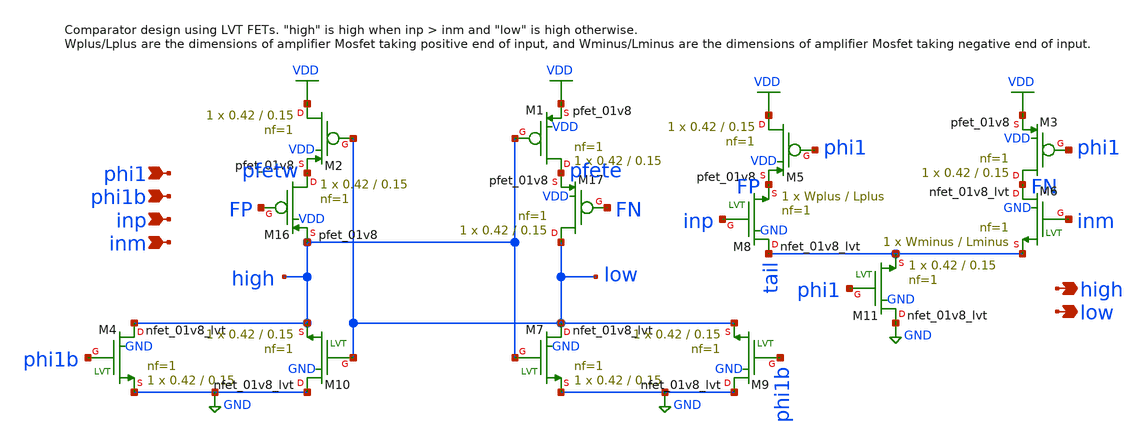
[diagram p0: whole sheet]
** sch_path: xschem/tryandtest/comparator_single_tail.sch
**.subckt comparator_single_tail phi1 high phi1b inp inm low
*.ipin phi1
*.opin high
*.ipin phi1b
*.ipin inp
*.ipin inm
*.opin low
XM1 pfete high VDD VDD sky130_fd_pr__pfet_01v8 L=0.15 W=0.42 nf=1 ad='int((nf+1)/2) * W/nf * 0.29' as='int((nf+2)/2) * W/nf * 0.29'
+ pd='2*int((nf+1)/2) * (W/nf + 0.29)' ps='2*int((nf+2)/2) * (W/nf + 0.29)' nrd='0.29 / W' nrs='0.29 / W'
+ sa=0 sb=0 sd=0 mult=1 m=1
XM2 VDD low pfetw VDD sky130_fd_pr__pfet_01v8 L=0.15 W=0.42 nf=1 ad='int((nf+1)/2) * W/nf * 0.29' as='int((nf+2)/2) * W/nf * 0.29'
+ pd='2*int((nf+1)/2) * (W/nf + 0.29)' ps='2*int((nf+2)/2) * (W/nf + 0.29)' nrd='0.29 / W' nrs='0.29 / W'
+ sa=0 sb=0 sd=0 mult=1 m=1
XM16 pfetw FP high VDD sky130_fd_pr__pfet_01v8 L=0.15 W=0.42 nf=1 ad='int((nf+1)/2) * W/nf * 0.29' as='int((nf+2)/2) * W/nf * 0.29'
+ pd='2*int((nf+1)/2) * (W/nf + 0.29)' ps='2*int((nf+2)/2) * (W/nf + 0.29)' nrd='0.29 / W' nrs='0.29 / W'
+ sa=0 sb=0 sd=0 mult=1 m=1
XM17 low FN pfete VDD sky130_fd_pr__pfet_01v8 L=0.15 W=0.42 nf=1 ad='int((nf+1)/2) * W/nf * 0.29' as='int((nf+2)/2) * W/nf * 0.29'
+ pd='2*int((nf+1)/2) * (W/nf + 0.29)' ps='2*int((nf+2)/2) * (W/nf + 0.29)' nrd='0.29 / W' nrs='0.29 / W'
+ sa=0 sb=0 sd=0 mult=1 m=1
XM3 FN phi1 VDD VDD sky130_fd_pr__pfet_01v8 L=0.15 W=0.42 nf=1 ad='int((nf+1)/2) * W/nf * 0.29' as='int((nf+2)/2) * W/nf * 0.29'
+ pd='2*int((nf+1)/2) * (W/nf + 0.29)' ps='2*int((nf+2)/2) * (W/nf + 0.29)' nrd='0.29 / W' nrs='0.29 / W'
+ sa=0 sb=0 sd=0 mult=1 m=1
XM5 VDD phi1 FP VDD sky130_fd_pr__pfet_01v8 L=0.15 W=0.42 nf=1 ad='int((nf+1)/2) * W/nf * 0.29' as='int((nf+2)/2) * W/nf * 0.29'
+ pd='2*int((nf+1)/2) * (W/nf + 0.29)' ps='2*int((nf+2)/2) * (W/nf + 0.29)' nrd='0.29 / W' nrs='0.29 / W'
+ sa=0 sb=0 sd=0 mult=1 m=1
XM4 high phi1b GND GND sky130_fd_pr__nfet_01v8_lvt L=0.15 W=0.42 nf=1 ad='int((nf+1)/2) * W/nf * 0.29'
+ as='int((nf+2)/2) * W/nf * 0.29' pd='2*int((nf+1)/2) * (W/nf + 0.29)' ps='2*int((nf+2)/2) * (W/nf + 0.29)'
+ nrd='0.29 / W' nrs='0.29 / W' sa=0 sb=0 sd=0 mult=1 m=1
XM7 low high GND GND sky130_fd_pr__nfet_01v8_lvt L=0.15 W=0.42 nf=1 ad='int((nf+1)/2) * W/nf * 0.29'
+ as='int((nf+2)/2) * W/nf * 0.29' pd='2*int((nf+1)/2) * (W/nf + 0.29)' ps='2*int((nf+2)/2) * (W/nf + 0.29)'
+ nrd='0.29 / W' nrs='0.29 / W' sa=0 sb=0 sd=0 mult=1 m=1
XM8 tail inp FP GND sky130_fd_pr__nfet_01v8_lvt L=Lplus W=Wplus nf=1 ad='int((nf+1)/2) * W/nf * 0.29'
+ as='int((nf+2)/2) * W/nf * 0.29' pd='2*int((nf+1)/2) * (W/nf + 0.29)' ps='2*int((nf+2)/2) * (W/nf + 0.29)'
+ nrd='0.29 / W' nrs='0.29 / W' sa=0 sb=0 sd=0 mult=1 m=1
XM6 FN inm tail GND sky130_fd_pr__nfet_01v8_lvt L=Lminus W=Wminus nf=1 ad='int((nf+1)/2) * W/nf * 0.29'
+ as='int((nf+2)/2) * W/nf * 0.29' pd='2*int((nf+1)/2) * (W/nf + 0.29)' ps='2*int((nf+2)/2) * (W/nf + 0.29)'
+ nrd='0.29 / W' nrs='0.29 / W' sa=0 sb=0 sd=0 mult=1 m=1
XM9 GND phi1b low GND sky130_fd_pr__nfet_01v8_lvt L=0.15 W=0.42 nf=1 ad='int((nf+1)/2) * W/nf * 0.29'
+ as='int((nf+2)/2) * W/nf * 0.29' pd='2*int((nf+1)/2) * (W/nf + 0.29)' ps='2*int((nf+2)/2) * (W/nf + 0.29)'
+ nrd='0.29 / W' nrs='0.29 / W' sa=0 sb=0 sd=0 mult=1 m=1
XM10 GND low high GND sky130_fd_pr__nfet_01v8_lvt L=0.15 W=0.42 nf=1 ad='int((nf+1)/2) * W/nf * 0.29'
+ as='int((nf+2)/2) * W/nf * 0.29' pd='2*int((nf+1)/2) * (W/nf + 0.29)' ps='2*int((nf+2)/2) * (W/nf + 0.29)'
+ nrd='0.29 / W' nrs='0.29 / W' sa=0 sb=0 sd=0 mult=1 m=1
XM11 GND phi1 tail GND sky130_fd_pr__nfet_01v8_lvt L=0.15 W=0.42 nf=1 ad='int((nf+1)/2) * W/nf * 0.29'
+ as='int((nf+2)/2) * W/nf * 0.29' pd='2*int((nf+1)/2) * (W/nf + 0.29)' ps='2*int((nf+2)/2) * (W/nf + 0.29)'
+ nrd='0.29 / W' nrs='0.29 / W' sa=0 sb=0 sd=0 mult=1 m=1
**.ends
.GLOBAL VDD
.GLOBAL GND
.end
